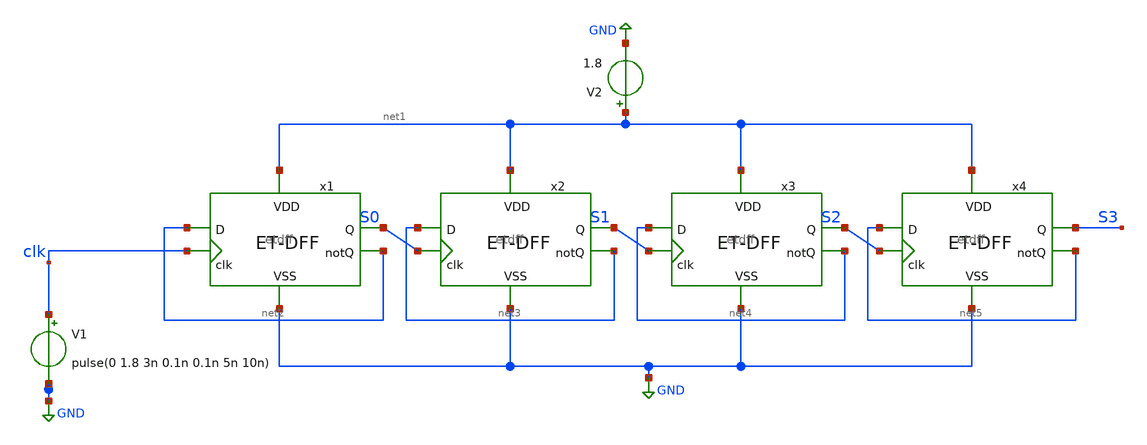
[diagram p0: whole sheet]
** sch_path: Layouts and Schematics/Spice Sim and Schem/counttest.sch
**.subckt counttest
V1 clk GND pulse(0 1.8 3n 0.1n 0.1n 5n 10n)
V2 net1 GND 1.8
x1 net1 net2 S0 clk net2 GND etdff
x2 net1 net3 S1 S0 net3 GND etdff
x3 net1 net4 S2 S1 net4 GND etdff
x4 net1 net5 S3 S2 net5 GND etdff
**** begin user architecture code
 .lib $::SKYWATER_MODELS/sky130.lib.spice tt

.include /home/wyatt/EE431
.tran 1n 400n
.control
run
.endc

**** end user architecture code
**.ends
.GLOBAL GND
.end
